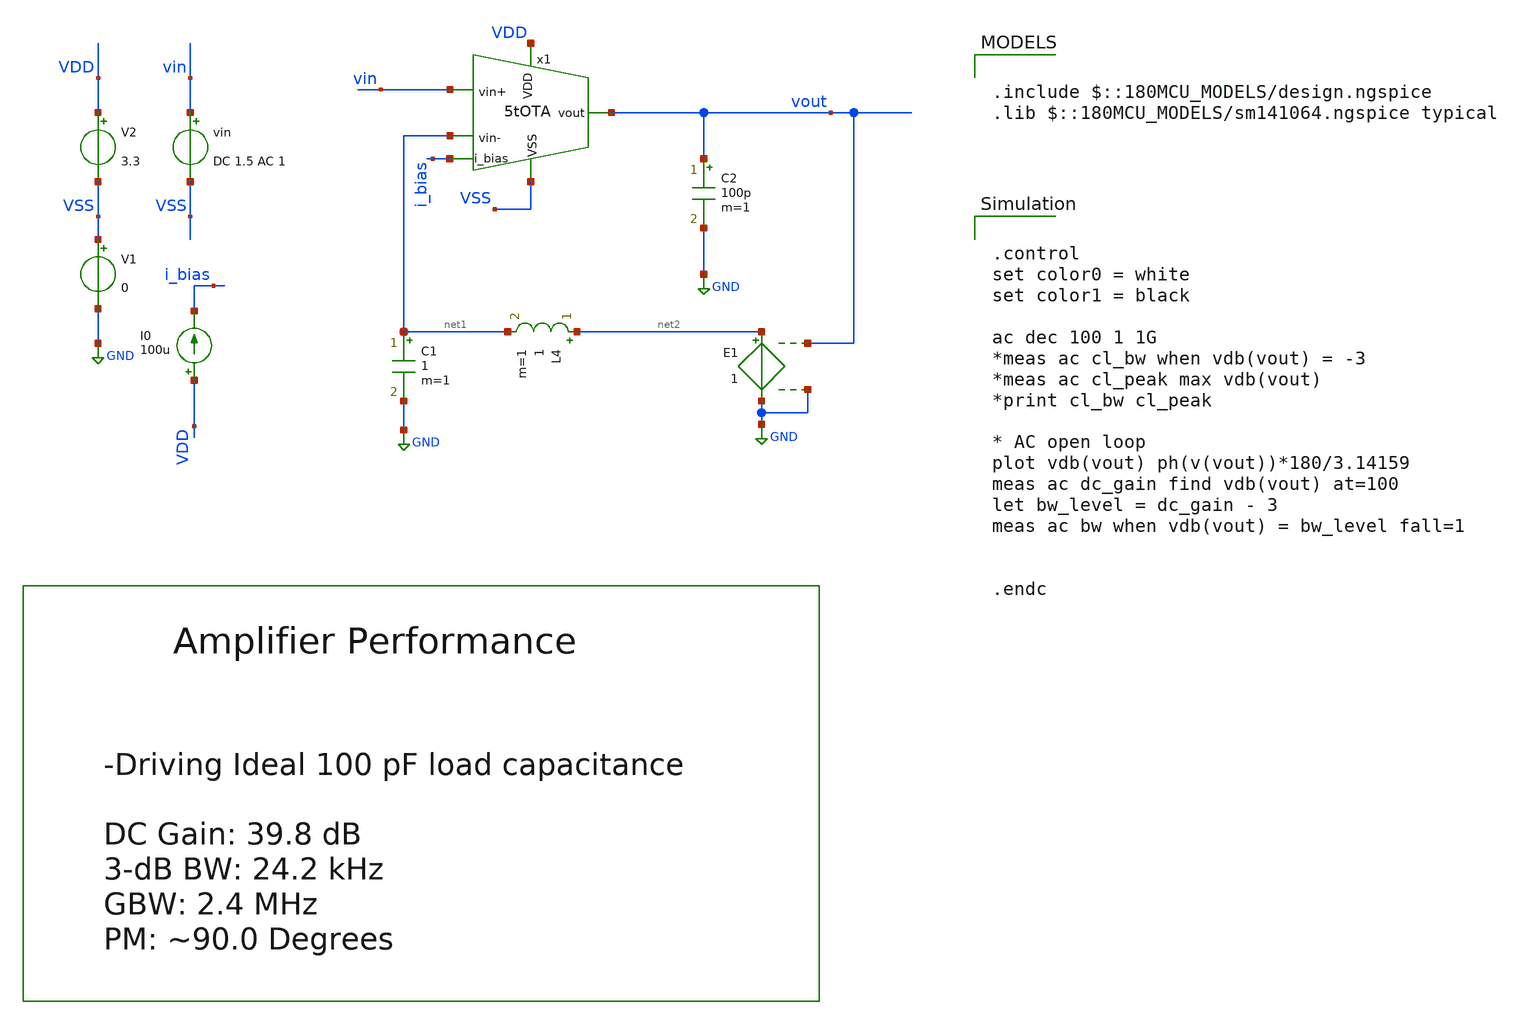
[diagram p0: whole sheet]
** sch_path: designs/libs/core_amps/ota_5t/tb/5tOTA_tb_ac.sch
**.subckt 5tOTA_tb_ac
V1 VSS GND 0
V2 VDD VSS 3.3
I0 VDD i_bias 100u
vin vin VSS DC 1.5 AC 1
C2 vout GND 100p m=1
L4 net2 net1 1 m=1
E1 net2 GND vout GND 1
C1 net1 GND 1 m=1
x1 VDD vout vin net1 i_bias VSS 5tOTA
**** begin user architecture code

.include $::180MCU_MODELS/design.ngspice
.lib $::180MCU_MODELS/sm141064.ngspice typical



.control
set color0 = white
set color1 = black

ac dec 100 1 1G
*meas ac cl_bw when vdb(vout) = -3
*meas ac cl_peak max vdb(vout)
*print cl_bw cl_peak

* AC open loop
plot vdb(vout) ph(v(vout))*180/3.14159
meas ac dc_gain find vdb(vout) at=100
let bw_level = dc_gain - 3
meas ac bw when vdb(vout) = bw_level fall=1


.endc


**** end user architecture code
**.ends

* expanding   symbol:  libs/core_amps/ota_5t/schem/5tOTA.sym # of pins=6
** sym_path: designs/5tOTA.sym
** sch_path: designs/5tOTA.sch
.subckt 5tOTA VDD vout vin+ vin- i_bias VSS
*.ipin VDD
*.opin vout
*.ipin i_bias
*.ipin vin+
*.ipin vin-
*.ipin VSS
XM1 net1 vin+ net2 VSS nfet_03v3 L=0.5u W=11.43u nf=1 ad='int((nf+1)/2) * W/nf * 0.18u' as='int((nf+2)/2) * W/nf * 0.18u'
+ pd='2*int((nf+1)/2) * (W/nf + 0.18u)' ps='2*int((nf+2)/2) * (W/nf + 0.18u)' nrd='0.18u / W' nrs='0.18u / W'
+ sa=0 sb=0 sd=0 m=1
XM2 vout vin- net2 VSS nfet_03v3 L=0.5u W=11.43u nf=1 ad='int((nf+1)/2) * W/nf * 0.18u' as='int((nf+2)/2) * W/nf * 0.18u'
+ pd='2*int((nf+1)/2) * (W/nf + 0.18u)' ps='2*int((nf+2)/2) * (W/nf + 0.18u)' nrd='0.18u / W' nrs='0.18u / W'
+ sa=0 sb=0 sd=0 m=1
XM3 net1 net1 VDD VDD pfet_03v3 L=0.5u W=22.86u nf=1 ad='int((nf+1)/2) * W/nf * 0.18u' as='int((nf+2)/2) * W/nf * 0.18u'
+ pd='2*int((nf+1)/2) * (W/nf + 0.18u)' ps='2*int((nf+2)/2) * (W/nf + 0.18u)' nrd='0.18u / W' nrs='0.18u / W'
+ sa=0 sb=0 sd=0 m=1
XM4 vout net1 VDD VDD pfet_03v3 L=0.5u W=22.86u nf=1 ad='int((nf+1)/2) * W/nf * 0.18u' as='int((nf+2)/2) * W/nf * 0.18u'
+ pd='2*int((nf+1)/2) * (W/nf + 0.18u)' ps='2*int((nf+2)/2) * (W/nf + 0.18u)' nrd='0.18u / W' nrs='0.18u / W'
+ sa=0 sb=0 sd=0 m=1
XM5 net2 i_bias VSS VSS nfet_03v3 L=0.5u W=22.86u nf=1 ad='int((nf+1)/2) * W/nf * 0.18u' as='int((nf+2)/2) * W/nf * 0.18u'
+ pd='2*int((nf+1)/2) * (W/nf + 0.18u)' ps='2*int((nf+2)/2) * (W/nf + 0.18u)' nrd='0.18u / W' nrs='0.18u / W'
+ sa=0 sb=0 sd=0 m=1
XM6 i_bias i_bias VSS VSS nfet_03v3 L=0.5u W=22.86u nf=1 ad='int((nf+1)/2) * W/nf * 0.18u' as='int((nf+2)/2) * W/nf * 0.18u'
+ pd='2*int((nf+1)/2) * (W/nf + 0.18u)' ps='2*int((nf+2)/2) * (W/nf + 0.18u)' nrd='0.18u / W' nrs='0.18u / W'
+ sa=0 sb=0 sd=0 m=1
.ends

.GLOBAL GND
.end
